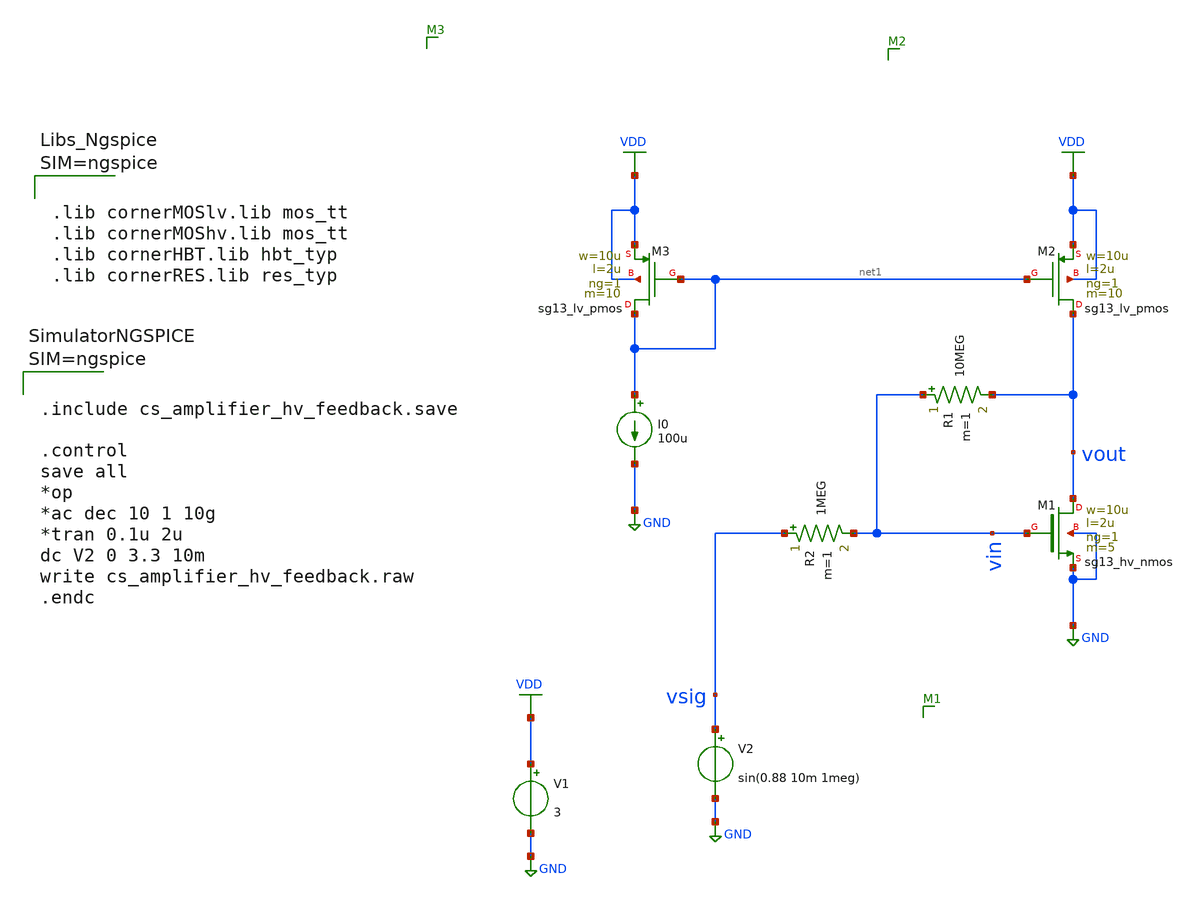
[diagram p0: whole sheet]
** sch_path: Schematics/lab_1/cs_amplifier_hv_feedback.sch
**.subckt cs_amplifier_hv_feedback
V1 VDD GND 3
V2 vsig GND sin(0.88 10m 1meg)
XM1 vout vin GND GND sg13_hv_nmos w=10u l=2u ng=1 m=5 mm_ok=1
R2 vsig vin 1MEG m=1
XM2 vout net1 VDD VDD sg13_lv_pmos w=10u l=2u ng=1 m=10 mm_ok=1
I0 net1 GND 100u
R1 vin vout 10MEG m=1
XM3 net1 net1 VDD VDD sg13_lv_pmos w=10u l=2u ng=1 m=10 mm_ok=1
**** begin user architecture code



.lib cornerMOSlv.lib mos_tt
.lib cornerMOShv.lib mos_tt
.lib cornerHBT.lib hbt_typ
.lib cornerRES.lib res_typ






.include cs_amplifier_hv_feedback.save

.control
save all
*op
*ac dec 10 1 10g
*tran 0.1u 2u
dc V2 0 3.3 10m
write cs_amplifier_hv_feedback.raw
.endc



**** end user architecture code
**.ends
.GLOBAL GND
.GLOBAL VDD
.end
